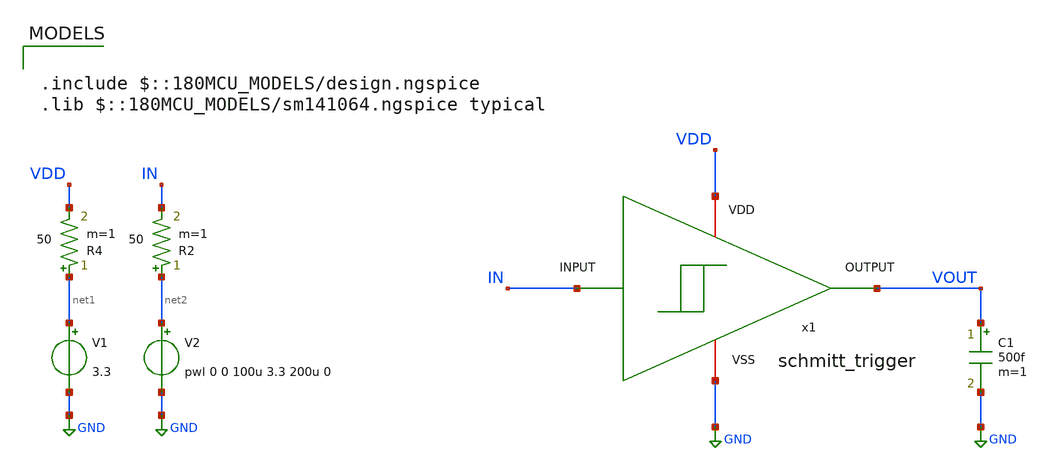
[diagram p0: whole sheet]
** sch_path: designs/schmitt_trigger/schmitt_trigger_tb_tran.sch
**.subckt schmitt_trigger_tb_tran
V1 net1 GND 3.3
V2 net2 GND pwl 0 0 100u 3.3 200u 0
C1 VOUT GND 500f m=1
R2 net2 IN 50 m=1
R4 net1 VDD 50 m=1
x1 VDD IN VOUT GND schmitt_trigger
**** begin user architecture code

.include $::180MCU_MODELS/design.ngspice
.lib $::180MCU_MODELS/sm141064.ngspice typical




.control
save all

** Simulación transitoria
tran 1u 200u

setplot tran1
let vin  = v(IN)
let vout = v(VOUT)

meas tran vin_fall FIND v(IN) WHEN v(VOUT)=1.65 FALL=1
meas tran vin_rise FIND v(IN) WHEN v(VOUT)=1.65 RISE=1

let diff = abs(vin_fall-vin_rise)
print diff

plot vout vin

write comparator_tb_tran.raw
.endc


**** end user architecture code
**.ends

* expanding   symbol:  gf180/schmitt_trigger/schmitt_trigger.sym # of pins=4
** sym_path: designs/schmitt_trigger/schmitt_trigger.sym
** sch_path: designs/schmitt_trigger/schmitt_trigger.sch
.subckt schmitt_trigger VDD INPUT OUTPUT VSS
*.ipin INPUT
*.opin OUTPUT
*.iopin VSS
*.iopin VDD
XM1 net2 INPUT net3 VSS nfet_03v3 L=0.28u W=2u nf=1 ad='int((nf+1)/2) * W/nf * 0.18u' as='int((nf+2)/2) * W/nf * 0.18u'
+ pd='2*int((nf+1)/2) * (W/nf + 0.18u)' ps='2*int((nf+2)/2) * (W/nf + 0.18u)' nrd='0.18u / W' nrs='0.18u / W'
+ sa=0 sb=0 sd=0 m=1
XM2 net3 INPUT VSS VSS nfet_03v3 L=0.28u W=2u nf=1 ad='int((nf+1)/2) * W/nf * 0.18u' as='int((nf+2)/2) * W/nf * 0.18u'
+ pd='2*int((nf+1)/2) * (W/nf + 0.18u)' ps='2*int((nf+2)/2) * (W/nf + 0.18u)' nrd='0.18u / W' nrs='0.18u / W'
+ sa=0 sb=0 sd=0 m=1
XM3 net2 INPUT net1 VDD pfet_03v3 L=0.28u W=6u nf=1 ad='int((nf+1)/2) * W/nf * 0.18u' as='int((nf+2)/2) * W/nf * 0.18u'
+ pd='2*int((nf+1)/2) * (W/nf + 0.18u)' ps='2*int((nf+2)/2) * (W/nf + 0.18u)' nrd='0.18u / W' nrs='0.18u / W'
+ sa=0 sb=0 sd=0 m=1
XM4 net1 INPUT VDD VDD pfet_03v3 L=0.28u W=6u nf=1 ad='int((nf+1)/2) * W/nf * 0.18u' as='int((nf+2)/2) * W/nf * 0.18u'
+ pd='2*int((nf+1)/2) * (W/nf + 0.18u)' ps='2*int((nf+2)/2) * (W/nf + 0.18u)' nrd='0.18u / W' nrs='0.18u / W'
+ sa=0 sb=0 sd=0 m=1
XM5 VSS net2 net1 VDD pfet_03v3 L=0.56u W=1.5u nf=1 ad='int((nf+1)/2) * W/nf * 0.18u' as='int((nf+2)/2) * W/nf * 0.18u'
+ pd='2*int((nf+1)/2) * (W/nf + 0.18u)' ps='2*int((nf+2)/2) * (W/nf + 0.18u)' nrd='0.18u / W' nrs='0.18u / W'
+ sa=0 sb=0 sd=0 m=1
XM6 VDD net2 net3 VSS nfet_03v3 L=0.56u W=0.5u nf=1 ad='int((nf+1)/2) * W/nf * 0.18u' as='int((nf+2)/2) * W/nf * 0.18u'
+ pd='2*int((nf+1)/2) * (W/nf + 0.18u)' ps='2*int((nf+2)/2) * (W/nf + 0.18u)' nrd='0.18u / W' nrs='0.18u / W'
+ sa=0 sb=0 sd=0 m=1
XM7 OUTPUT net2 VDD VDD pfet_03v3 L=0.28u W=6u nf=1 ad='int((nf+1)/2) * W/nf * 0.18u' as='int((nf+2)/2) * W/nf * 0.18u'
+ pd='2*int((nf+1)/2) * (W/nf + 0.18u)' ps='2*int((nf+2)/2) * (W/nf + 0.18u)' nrd='0.18u / W' nrs='0.18u / W'
+ sa=0 sb=0 sd=0 m=1
XM8 OUTPUT net2 VSS VSS nfet_03v3 L=0.28u W=2u nf=1 ad='int((nf+1)/2) * W/nf * 0.18u' as='int((nf+2)/2) * W/nf * 0.18u'
+ pd='2*int((nf+1)/2) * (W/nf + 0.18u)' ps='2*int((nf+2)/2) * (W/nf + 0.18u)' nrd='0.18u / W' nrs='0.18u / W'
+ sa=0 sb=0 sd=0 m=1
.ends

.GLOBAL GND
.end
